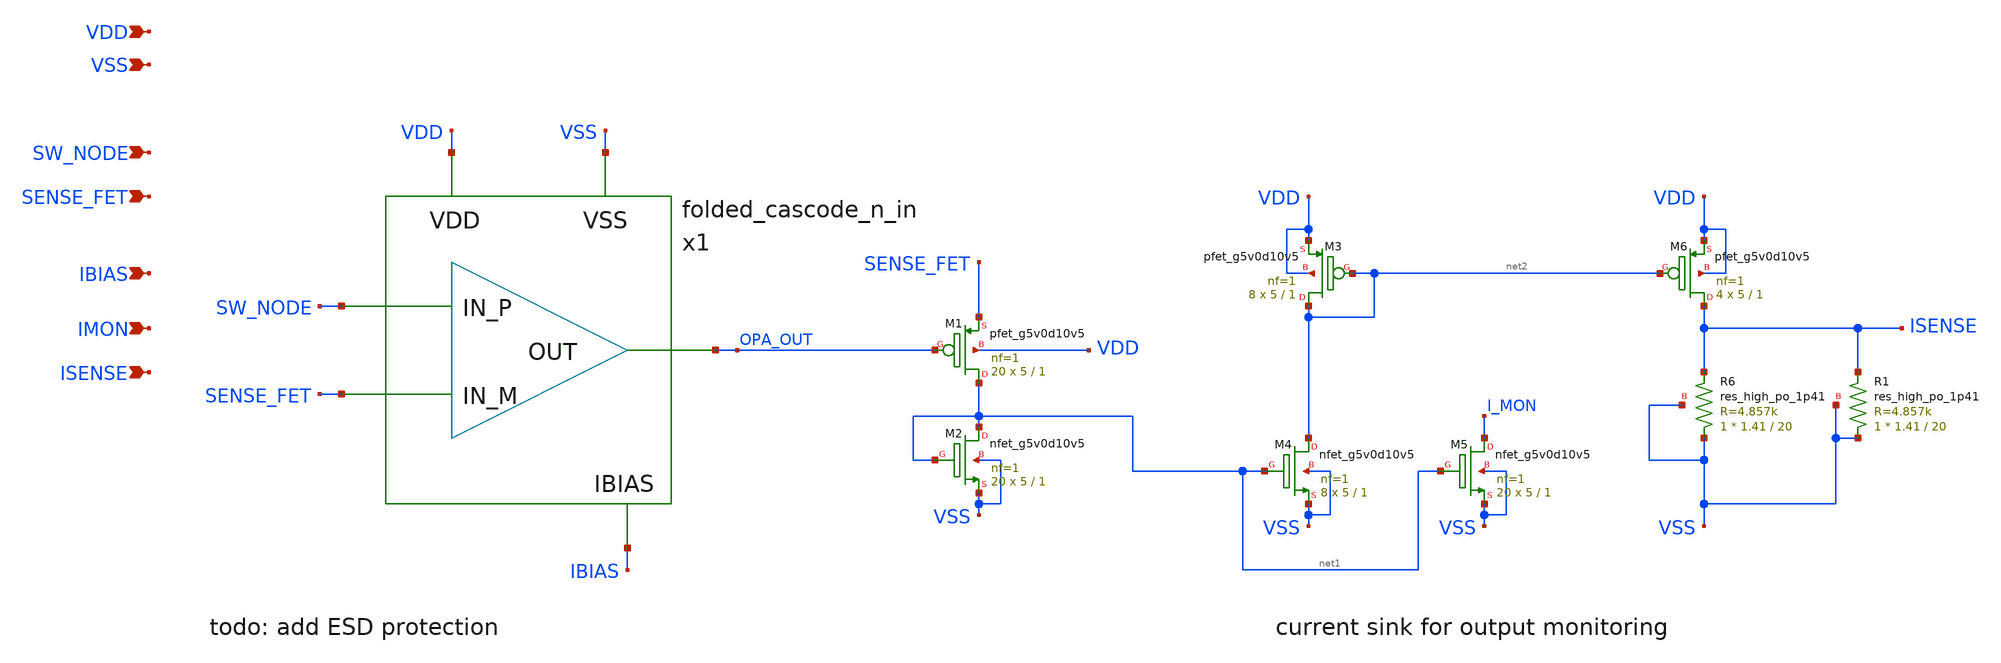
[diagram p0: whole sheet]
** sch_path: design/current-sense/current_sense.sch
**.subckt current_sense SW_NODE SENSE_FET VDD VSS IBIAS IMON ISENSE
*.ipin SW_NODE
*.ipin SENSE_FET
*.ipin VDD
*.ipin VSS
*.ipin IBIAS
*.ipin IMON
*.ipin ISENSE
x1 SW_NODE SENSE_FET OPA_OUT VDD VSS IBIAS folded_cascode_n_in
XM1 net1 OPA_OUT SENSE_FET VDD sky130_fd_pr__pfet_g5v0d10v5 L=1 W=5 nf=1 ad='int((nf+1)/2) * W/nf * 0.29'
+ as='int((nf+2)/2) * W/nf * 0.29' pd='2*int((nf+1)/2) * (W/nf + 0.29)' ps='2*int((nf+2)/2) * (W/nf + 0.29)'
+ nrd='0.29 / W' nrs='0.29 / W' sa=0 sb=0 sd=0 mult=20 m=20
XM2 net1 net1 VSS VSS sky130_fd_pr__nfet_g5v0d10v5 L=1 W=5 nf=1 ad='int((nf+1)/2) * W/nf * 0.29' as='int((nf+2)/2) * W/nf * 0.29'
+ pd='2*int((nf+1)/2) * (W/nf + 0.29)' ps='2*int((nf+2)/2) * (W/nf + 0.29)' nrd='0.29 / W' nrs='0.29 / W'
+ sa=0 sb=0 sd=0 mult=20 m=20
XM4 net2 net1 VSS VSS sky130_fd_pr__nfet_g5v0d10v5 L=1 W=5 nf=1 ad='int((nf+1)/2) * W/nf * 0.29' as='int((nf+2)/2) * W/nf * 0.29'
+ pd='2*int((nf+1)/2) * (W/nf + 0.29)' ps='2*int((nf+2)/2) * (W/nf + 0.29)' nrd='0.29 / W' nrs='0.29 / W'
+ sa=0 sb=0 sd=0 mult=8 m=8
XM3 net2 net2 VDD VDD sky130_fd_pr__pfet_g5v0d10v5 L=1 W=5 nf=1 ad='int((nf+1)/2) * W/nf * 0.29' as='int((nf+2)/2) * W/nf * 0.29'
+ pd='2*int((nf+1)/2) * (W/nf + 0.29)' ps='2*int((nf+2)/2) * (W/nf + 0.29)' nrd='0.29 / W' nrs='0.29 / W'
+ sa=0 sb=0 sd=0 mult=8 m=8
XM5 I_MON net1 VSS VSS sky130_fd_pr__nfet_g5v0d10v5 L=1 W=5 nf=1 ad='int((nf+1)/2) * W/nf * 0.29' as='int((nf+2)/2) * W/nf * 0.29'
+ pd='2*int((nf+1)/2) * (W/nf + 0.29)' ps='2*int((nf+2)/2) * (W/nf + 0.29)' nrd='0.29 / W' nrs='0.29 / W'
+ sa=0 sb=0 sd=0 mult=20 m=20
XM6 ISENSE net2 VDD VDD sky130_fd_pr__pfet_g5v0d10v5 L=1 W=5 nf=1 ad='int((nf+1)/2) * W/nf * 0.29' as='int((nf+2)/2) * W/nf * 0.29'
+ pd='2*int((nf+1)/2) * (W/nf + 0.29)' ps='2*int((nf+2)/2) * (W/nf + 0.29)' nrd='0.29 / W' nrs='0.29 / W'
+ sa=0 sb=0 sd=0 mult=4 m=4
XR6 VSS ISENSE VSS sky130_fd_pr__res_high_po_1p41 L=20 mult=1 m=1
XR1 VSS ISENSE VSS sky130_fd_pr__res_high_po_1p41 L=20 mult=1 m=1
**.ends

* expanding   symbol:  design/folded-cascode-n-in/folded_cascode_n_in.sym # of pins=6
** sym_path: design/folded-cascode-n-in/folded_cascode_n_in.sym
** sch_path: design/folded-cascode-n-in/folded_cascode_n_in.sch
.subckt folded_cascode_n_in IN_P IN_M OUT VDD VSS VBN
*.ipin IN_P
*.ipin IN_M
*.ipin OUT
*.ipin VDD
*.ipin VSS
*.ipin VBN
XM1 net1 VBN VSS VSS sky130_fd_pr__nfet_g5v0d10v5 L=1 W=5 nf=1 ad='int((nf+1)/2) * W/nf * 0.29' as='int((nf+2)/2) * W/nf * 0.29'
+ pd='2*int((nf+1)/2) * (W/nf + 0.29)' ps='2*int((nf+2)/2) * (W/nf + 0.29)' nrd='0.29 / W' nrs='0.29 / W'
+ sa=0 sb=0 sd=0 mult=12 m=12
XM3 VS1_P IN_M net1 VSS sky130_fd_pr__nfet_g5v0d10v5 L=1 W=5 nf=1 ad='int((nf+1)/2) * W/nf * 0.29' as='int((nf+2)/2) * W/nf * 0.29'
+ pd='2*int((nf+1)/2) * (W/nf + 0.29)' ps='2*int((nf+2)/2) * (W/nf + 0.29)' nrd='0.29 / W' nrs='0.29 / W'
+ sa=0 sb=0 sd=0 mult=24 m=24
XM4 VS1_M IN_P net1 VSS sky130_fd_pr__nfet_g5v0d10v5 L=1 W=5 nf=1 ad='int((nf+1)/2) * W/nf * 0.29' as='int((nf+2)/2) * W/nf * 0.29'
+ pd='2*int((nf+1)/2) * (W/nf + 0.29)' ps='2*int((nf+2)/2) * (W/nf + 0.29)' nrd='0.29 / W' nrs='0.29 / W'
+ sa=0 sb=0 sd=0 mult=24 m=24
XM9 net2 VCN net4 VSS sky130_fd_pr__nfet_g5v0d10v5 L=1 W=5 nf=1 ad='int((nf+1)/2) * W/nf * 0.29' as='int((nf+2)/2) * W/nf * 0.29'
+ pd='2*int((nf+1)/2) * (W/nf + 0.29)' ps='2*int((nf+2)/2) * (W/nf + 0.29)' nrd='0.29 / W' nrs='0.29 / W'
+ sa=0 sb=0 sd=0 mult=4 m=4
XM10 net3 net2 VSS VSS sky130_fd_pr__nfet_g5v0d10v5 L=1 W=5 nf=1 ad='int((nf+1)/2) * W/nf * 0.29' as='int((nf+2)/2) * W/nf * 0.29'
+ pd='2*int((nf+1)/2) * (W/nf + 0.29)' ps='2*int((nf+2)/2) * (W/nf + 0.29)' nrd='0.29 / W' nrs='0.29 / W'
+ sa=0 sb=0 sd=0 mult=4 m=4
XM11 net4 net2 VSS VSS sky130_fd_pr__nfet_g5v0d10v5 L=1 W=5 nf=1 ad='int((nf+1)/2) * W/nf * 0.29' as='int((nf+2)/2) * W/nf * 0.29'
+ pd='2*int((nf+1)/2) * (W/nf + 0.29)' ps='2*int((nf+2)/2) * (W/nf + 0.29)' nrd='0.29 / W' nrs='0.29 / W'
+ sa=0 sb=0 sd=0 mult=4 m=4
XM12 OUT VCN net3 VSS sky130_fd_pr__nfet_g5v0d10v5 L=1 W=5 nf=1 ad='int((nf+1)/2) * W/nf * 0.29' as='int((nf+2)/2) * W/nf * 0.29'
+ pd='2*int((nf+1)/2) * (W/nf + 0.29)' ps='2*int((nf+2)/2) * (W/nf + 0.29)' nrd='0.29 / W' nrs='0.29 / W'
+ sa=0 sb=0 sd=0 mult=4 m=4
XM5 VS1_P VBP_INT VDD VDD sky130_fd_pr__pfet_g5v0d10v5 L=1 W=5 nf=1 ad='int((nf+1)/2) * W/nf * 0.29'
+ as='int((nf+2)/2) * W/nf * 0.29' pd='2*int((nf+1)/2) * (W/nf + 0.29)' ps='2*int((nf+2)/2) * (W/nf + 0.29)'
+ nrd='0.29 / W' nrs='0.29 / W' sa=0 sb=0 sd=0 mult=10 m=10
XM13 VS1_M VBP_INT VDD VDD sky130_fd_pr__pfet_g5v0d10v5 L=1 W=5 nf=1 ad='int((nf+1)/2) * W/nf * 0.29'
+ as='int((nf+2)/2) * W/nf * 0.29' pd='2*int((nf+1)/2) * (W/nf + 0.29)' ps='2*int((nf+2)/2) * (W/nf + 0.29)'
+ nrd='0.29 / W' nrs='0.29 / W' sa=0 sb=0 sd=0 mult=10 m=10
XM17 VBP_INT VBN VSS VSS sky130_fd_pr__nfet_g5v0d10v5 L=1 W=5 nf=1 ad='int((nf+1)/2) * W/nf * 0.29' as='int((nf+2)/2) * W/nf * 0.29'
+ pd='2*int((nf+1)/2) * (W/nf + 0.29)' ps='2*int((nf+2)/2) * (W/nf + 0.29)' nrd='0.29 / W' nrs='0.29 / W'
+ sa=0 sb=0 sd=0 mult=1 m=1
XM18 VBP_INT VBP_INT VDD VDD sky130_fd_pr__pfet_g5v0d10v5 L=1 W=5 nf=1 ad='int((nf+1)/2) * W/nf * 0.29'
+ as='int((nf+2)/2) * W/nf * 0.29' pd='2*int((nf+1)/2) * (W/nf + 0.29)' ps='2*int((nf+2)/2) * (W/nf + 0.29)'
+ nrd='0.29 / W' nrs='0.29 / W' sa=0 sb=0 sd=0 mult=1 m=1
XM14 net2 VCP VS1_M VDD sky130_fd_pr__pfet_g5v0d10v5 L=1 W=5 nf=1 ad='int((nf+1)/2) * W/nf * 0.29' as='int((nf+2)/2) * W/nf * 0.29'
+ pd='2*int((nf+1)/2) * (W/nf + 0.29)' ps='2*int((nf+2)/2) * (W/nf + 0.29)' nrd='0.29 / W' nrs='0.29 / W'
+ sa=0 sb=0 sd=0 mult=4 m=4
XM19 OUT VCP VS1_P VDD sky130_fd_pr__pfet_g5v0d10v5 L=1 W=5 nf=1 ad='int((nf+1)/2) * W/nf * 0.29' as='int((nf+2)/2) * W/nf * 0.29'
+ pd='2*int((nf+1)/2) * (W/nf + 0.29)' ps='2*int((nf+2)/2) * (W/nf + 0.29)' nrd='0.29 / W' nrs='0.29 / W'
+ sa=0 sb=0 sd=0 mult=4 m=4
XM2 VBP_INT VBP_INT VS1_P VSS sky130_fd_pr__nfet_g5v0d10v5 L=1 W=5 nf=1 ad='int((nf+1)/2) * W/nf * 0.29'
+ as='int((nf+2)/2) * W/nf * 0.29' pd='2*int((nf+1)/2) * (W/nf + 0.29)' ps='2*int((nf+2)/2) * (W/nf + 0.29)'
+ nrd='0.29 / W' nrs='0.29 / W' sa=0 sb=0 sd=0 mult=1 m=1
XM6 VBP_INT VBP_INT VS1_M VSS sky130_fd_pr__nfet_g5v0d10v5 L=1 W=5 nf=1 ad='int((nf+1)/2) * W/nf * 0.29'
+ as='int((nf+2)/2) * W/nf * 0.29' pd='2*int((nf+1)/2) * (W/nf + 0.29)' ps='2*int((nf+2)/2) * (W/nf + 0.29)'
+ nrd='0.29 / W' nrs='0.29 / W' sa=0 sb=0 sd=0 mult=1 m=1
XM7 VBP VBP VDD VDD sky130_fd_pr__pfet_g5v0d10v5 L=1 W=5 nf=1 ad='int((nf+1)/2) * W/nf * 0.29' as='int((nf+2)/2) * W/nf * 0.29'
+ pd='2*int((nf+1)/2) * (W/nf + 0.29)' ps='2*int((nf+2)/2) * (W/nf + 0.29)' nrd='0.29 / W' nrs='0.29 / W'
+ sa=0 sb=0 sd=0 mult=1 m=1
XM8 net5 VBP net12 VDD sky130_fd_pr__pfet_g5v0d10v5 L=1 W=5 nf=1 ad='int((nf+1)/2) * W/nf * 0.29' as='int((nf+2)/2) * W/nf * 0.29'
+ pd='2*int((nf+1)/2) * (W/nf + 0.29)' ps='2*int((nf+2)/2) * (W/nf + 0.29)' nrd='0.29 / W' nrs='0.29 / W'
+ sa=0 sb=0 sd=0 mult=1 m=1
XM15 VCN VBP VDD VDD sky130_fd_pr__pfet_g5v0d10v5 L=1 W=5 nf=1 ad='int((nf+1)/2) * W/nf * 0.29' as='int((nf+2)/2) * W/nf * 0.29'
+ pd='2*int((nf+1)/2) * (W/nf + 0.29)' ps='2*int((nf+2)/2) * (W/nf + 0.29)' nrd='0.29 / W' nrs='0.29 / W'
+ sa=0 sb=0 sd=0 mult=1 m=1
XM16 net5 net5 net6 VSS sky130_fd_pr__nfet_g5v0d10v5 L=1 W=5 nf=1 ad='int((nf+1)/2) * W/nf * 0.29' as='int((nf+2)/2) * W/nf * 0.29'
+ pd='2*int((nf+1)/2) * (W/nf + 0.29)' ps='2*int((nf+2)/2) * (W/nf + 0.29)' nrd='0.29 / W' nrs='0.29 / W'
+ sa=0 sb=0 sd=0 mult=2 m=2
XM20 net6 net5 VSS VSS sky130_fd_pr__nfet_g5v0d10v5 L=1 W=5 nf=1 ad='int((nf+1)/2) * W/nf * 0.29' as='int((nf+2)/2) * W/nf * 0.29'
+ pd='2*int((nf+1)/2) * (W/nf + 0.29)' ps='2*int((nf+2)/2) * (W/nf + 0.29)' nrd='0.29 / W' nrs='0.29 / W'
+ sa=0 sb=0 sd=0 mult=1 m=1
XM21 VCN VCN net6 VSS sky130_fd_pr__nfet_g5v0d10v5 L=1 W=5 nf=1 ad='int((nf+1)/2) * W/nf * 0.29' as='int((nf+2)/2) * W/nf * 0.29'
+ pd='2*int((nf+1)/2) * (W/nf + 0.29)' ps='2*int((nf+2)/2) * (W/nf + 0.29)' nrd='0.29 / W' nrs='0.29 / W'
+ sa=0 sb=0 sd=0 mult=1 m=1
XM24 net7 VBN net10 VSS sky130_fd_pr__nfet_g5v0d10v5 L=1 W=5 nf=1 ad='int((nf+1)/2) * W/nf * 0.29' as='int((nf+2)/2) * W/nf * 0.29'
+ pd='2*int((nf+1)/2) * (W/nf + 0.29)' ps='2*int((nf+2)/2) * (W/nf + 0.29)' nrd='0.29 / W' nrs='0.29 / W'
+ sa=0 sb=0 sd=0 mult=1 m=1
XM25 VCP VBN VSS VSS sky130_fd_pr__nfet_g5v0d10v5 L=1 W=5 nf=1 ad='int((nf+1)/2) * W/nf * 0.29' as='int((nf+2)/2) * W/nf * 0.29'
+ pd='2*int((nf+1)/2) * (W/nf + 0.29)' ps='2*int((nf+2)/2) * (W/nf + 0.29)' nrd='0.29 / W' nrs='0.29 / W'
+ sa=0 sb=0 sd=0 mult=1 m=1
XM26 net7 net7 net8 VDD sky130_fd_pr__pfet_g5v0d10v5 L=1 W=5 nf=1 ad='int((nf+1)/2) * W/nf * 0.29' as='int((nf+2)/2) * W/nf * 0.29'
+ pd='2*int((nf+1)/2) * (W/nf + 0.29)' ps='2*int((nf+2)/2) * (W/nf + 0.29)' nrd='0.29 / W' nrs='0.29 / W'
+ sa=0 sb=0 sd=0 mult=2 m=2
XM27 VCP VCP net8 VDD sky130_fd_pr__pfet_g5v0d10v5 L=1 W=5 nf=1 ad='int((nf+1)/2) * W/nf * 0.29' as='int((nf+2)/2) * W/nf * 0.29'
+ pd='2*int((nf+1)/2) * (W/nf + 0.29)' ps='2*int((nf+2)/2) * (W/nf + 0.29)' nrd='0.29 / W' nrs='0.29 / W'
+ sa=0 sb=0 sd=0 mult=1 m=1
XM28 net8 net7 VDD VDD sky130_fd_pr__pfet_g5v0d10v5 L=1 W=5 nf=1 ad='int((nf+1)/2) * W/nf * 0.29' as='int((nf+2)/2) * W/nf * 0.29'
+ pd='2*int((nf+1)/2) * (W/nf + 0.29)' ps='2*int((nf+2)/2) * (W/nf + 0.29)' nrd='0.29 / W' nrs='0.29 / W'
+ sa=0 sb=0 sd=0 mult=1 m=1
XM29 VBP VBN VSS VSS sky130_fd_pr__nfet_g5v0d10v5 L=1 W=5 nf=1 ad='int((nf+1)/2) * W/nf * 0.29' as='int((nf+2)/2) * W/nf * 0.29'
+ pd='2*int((nf+1)/2) * (W/nf + 0.29)' ps='2*int((nf+2)/2) * (W/nf + 0.29)' nrd='0.29 / W' nrs='0.29 / W'
+ sa=0 sb=0 sd=0 mult=1 m=1
XM32 net12 VBP net9 VDD sky130_fd_pr__pfet_g5v0d10v5 L=1 W=5 nf=1 ad='int((nf+1)/2) * W/nf * 0.29' as='int((nf+2)/2) * W/nf * 0.29'
+ pd='2*int((nf+1)/2) * (W/nf + 0.29)' ps='2*int((nf+2)/2) * (W/nf + 0.29)' nrd='0.29 / W' nrs='0.29 / W'
+ sa=0 sb=0 sd=0 mult=1 m=1
XM33 net9 VBP VDD VDD sky130_fd_pr__pfet_g5v0d10v5 L=1 W=5 nf=1 ad='int((nf+1)/2) * W/nf * 0.29' as='int((nf+2)/2) * W/nf * 0.29'
+ pd='2*int((nf+1)/2) * (W/nf + 0.29)' ps='2*int((nf+2)/2) * (W/nf + 0.29)' nrd='0.29 / W' nrs='0.29 / W'
+ sa=0 sb=0 sd=0 mult=1 m=1
XM34 net10 VBN net11 VSS sky130_fd_pr__nfet_g5v0d10v5 L=1 W=5 nf=1 ad='int((nf+1)/2) * W/nf * 0.29' as='int((nf+2)/2) * W/nf * 0.29'
+ pd='2*int((nf+1)/2) * (W/nf + 0.29)' ps='2*int((nf+2)/2) * (W/nf + 0.29)' nrd='0.29 / W' nrs='0.29 / W'
+ sa=0 sb=0 sd=0 mult=1 m=1
XM35 net11 VBN VSS VSS sky130_fd_pr__nfet_g5v0d10v5 L=1 W=5 nf=1 ad='int((nf+1)/2) * W/nf * 0.29' as='int((nf+2)/2) * W/nf * 0.29'
+ pd='2*int((nf+1)/2) * (W/nf + 0.29)' ps='2*int((nf+2)/2) * (W/nf + 0.29)' nrd='0.29 / W' nrs='0.29 / W'
+ sa=0 sb=0 sd=0 mult=1 m=1
XM30 VBN VBN VSS VSS sky130_fd_pr__nfet_g5v0d10v5 L=1 W=5 nf=1 ad='int((nf+1)/2) * W/nf * 0.29' as='int((nf+2)/2) * W/nf * 0.29'
+ pd='2*int((nf+1)/2) * (W/nf + 0.29)' ps='2*int((nf+2)/2) * (W/nf + 0.29)' nrd='0.29 / W' nrs='0.29 / W'
+ sa=0 sb=0 sd=0 mult=1 m=1
.ends

.end
